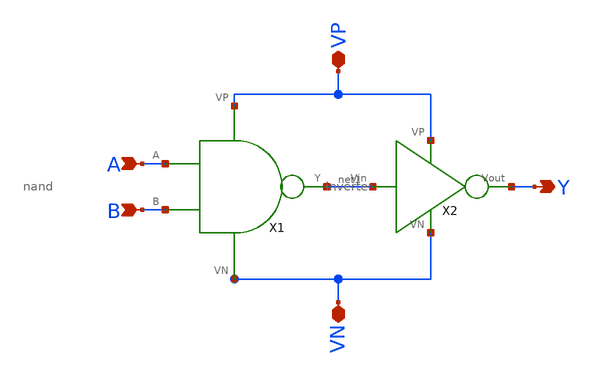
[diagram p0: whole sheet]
** sch_path: mini_proj_1/schematic/and.sch
**.subckt and A B VP VN Y
*.ipin A
*.ipin B
*.iopin VP
*.iopin VN
*.opin Y
X1 net1 A B VP VN nand
X2 VP VN net1 Y inverter
**.ends

* expanding   symbol:  /home/madvlsi/Documents/madvlsi/mini_proj_1/schematic/nand.sym # of pins=5
** sym_path: mini_proj_1/schematic/nand.sym
** sch_path: mini_proj_1/schematic/nand.sch
.subckt nand Y A B VP VN
*.ipin A
*.ipin B
*.iopin VP
*.iopin VN
*.opin Y
XM1 Y A VP VP sky130_fd_pr__pfet_01v8 L=0.15 W=1 nf=1 ad='int((nf+1)/2) * W/nf * 0.29' as='int((nf+2)/2) * W/nf * 0.29'
+ pd='2*int((nf+1)/2) * (W/nf + 0.29)' ps='2*int((nf+2)/2) * (W/nf + 0.29)' nrd='0.29 / W' nrs='0.29 / W'
+ sa=0 sb=0 sd=0 mult=1 m=1
XM2 VP B Y VP sky130_fd_pr__pfet_01v8 L=0.15 W=1 nf=1 ad='int((nf+1)/2) * W/nf * 0.29' as='int((nf+2)/2) * W/nf * 0.29'
+ pd='2*int((nf+1)/2) * (W/nf + 0.29)' ps='2*int((nf+2)/2) * (W/nf + 0.29)' nrd='0.29 / W' nrs='0.29 / W'
+ sa=0 sb=0 sd=0 mult=1 m=1
XM3 Y A net1 net1 sky130_fd_pr__nfet_01v8 L=0.15 W=1 nf=1 ad='int((nf+1)/2) * W/nf * 0.29' as='int((nf+2)/2) * W/nf * 0.29'
+ pd='2*int((nf+1)/2) * (W/nf + 0.29)' ps='2*int((nf+2)/2) * (W/nf + 0.29)' nrd='0.29 / W' nrs='0.29 / W'
+ sa=0 sb=0 sd=0 mult=1 m=1
XM4 VN B net1 VN sky130_fd_pr__nfet_01v8 L=0.15 W=1 nf=1 ad='int((nf+1)/2) * W/nf * 0.29' as='int((nf+2)/2) * W/nf * 0.29'
+ pd='2*int((nf+1)/2) * (W/nf + 0.29)' ps='2*int((nf+2)/2) * (W/nf + 0.29)' nrd='0.29 / W' nrs='0.29 / W'
+ sa=0 sb=0 sd=0 mult=1 m=1
.ends


* expanding   symbol:  /home/madvlsi/Documents/madvlsi/mini_proj_1/schematic/inverter.sym # of
*+ pins=4
** sym_path: mini_proj_1/schematic/inverter.sym
** sch_path: mini_proj_1/schematic/inverter.sch
.subckt inverter VP VN Vin Vout
*.ipin Vin
*.iopin VP
*.iopin VN
*.opin Vout
XM1 Vout Vin VN VN sky130_fd_pr__nfet_01v8 L=0.15 W=1 nf=1 ad='int((nf+1)/2) * W/nf * 0.29' as='int((nf+2)/2) * W/nf * 0.29'
+ pd='2*int((nf+1)/2) * (W/nf + 0.29)' ps='2*int((nf+2)/2) * (W/nf + 0.29)' nrd='0.29 / W' nrs='0.29 / W'
+ sa=0 sb=0 sd=0 mult=1 m=1
XM2 Vout Vin VP VP sky130_fd_pr__pfet_01v8 L=0.15 W=1 nf=1 ad='int((nf+1)/2) * W/nf * 0.29' as='int((nf+2)/2) * W/nf * 0.29'
+ pd='2*int((nf+1)/2) * (W/nf + 0.29)' ps='2*int((nf+2)/2) * (W/nf + 0.29)' nrd='0.29 / W' nrs='0.29 / W'
+ sa=0 sb=0 sd=0 mult=1 m=1
.ends

.end
